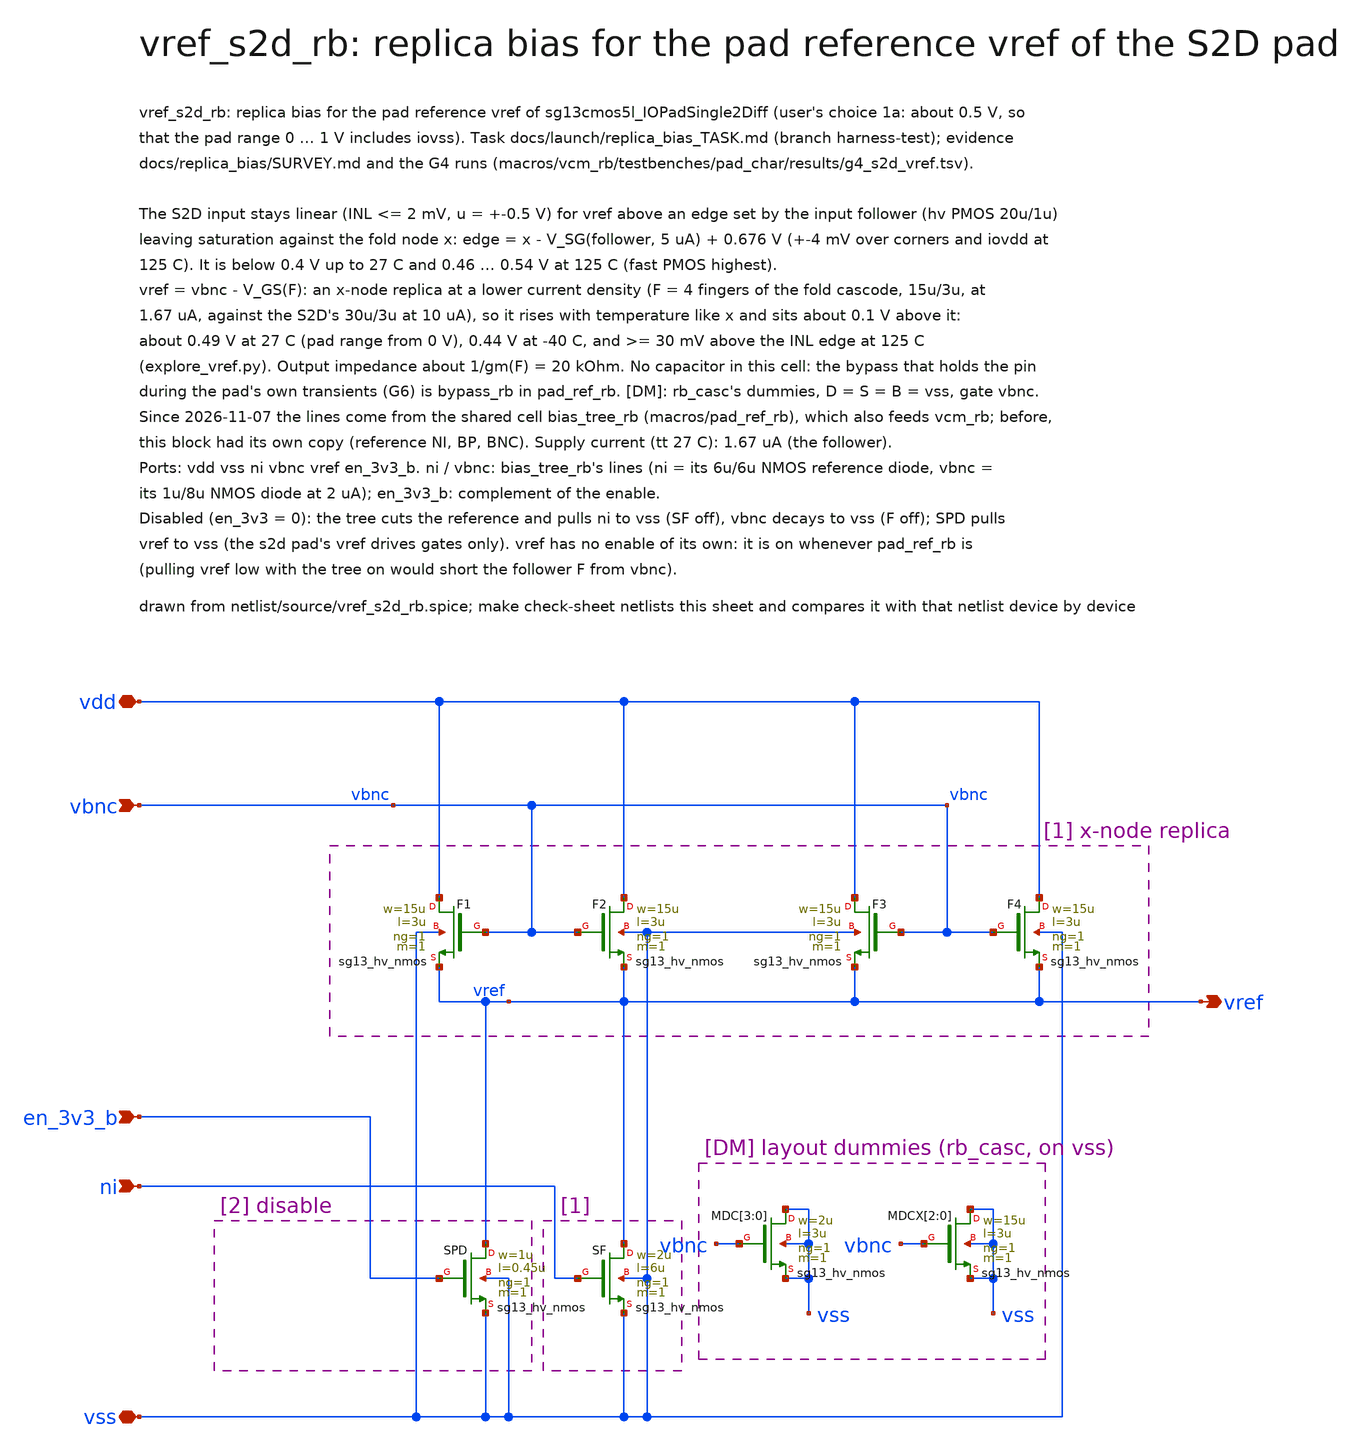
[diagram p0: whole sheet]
** sch_path: macros/vref_s2d_rb/schematic/xschem/vref_s2d_rb.sch
**.subckt vref_s2d_rb vdd vss ni vbnc vref en_3v3_b
*.iopin vdd
*.iopin vss
*.ipin ni
*.ipin vbnc
*.opin vref
*.ipin en_3v3_b
XF1 vdd vbnc vref vss sg13_hv_nmos w=15u l=3u ng=1 m=1 mm_ok=1
XF2 vdd vbnc vref vss sg13_hv_nmos w=15u l=3u ng=1 m=1 mm_ok=1
XF3 vdd vbnc vref vss sg13_hv_nmos w=15u l=3u ng=1 m=1 mm_ok=1
XF4 vdd vbnc vref vss sg13_hv_nmos w=15u l=3u ng=1 m=1 mm_ok=1
XSF vref ni vss vss sg13_hv_nmos w=2u l=6u ng=1 m=1 mm_ok=1
XSPD vref en_3v3_b vss vss sg13_hv_nmos w=1u l=0.45u ng=1 m=1 mm_ok=1
XMDC[3] vss vbnc vss vss sg13_hv_nmos w=2u l=3u ng=1 m=1 mm_ok=1
XMDC[2] vss vbnc vss vss sg13_hv_nmos w=2u l=3u ng=1 m=1 mm_ok=1
XMDC[1] vss vbnc vss vss sg13_hv_nmos w=2u l=3u ng=1 m=1 mm_ok=1
XMDC[0] vss vbnc vss vss sg13_hv_nmos w=2u l=3u ng=1 m=1 mm_ok=1
XMDCX[2] vss vbnc vss vss sg13_hv_nmos w=15u l=3u ng=1 m=1 mm_ok=1
XMDCX[1] vss vbnc vss vss sg13_hv_nmos w=15u l=3u ng=1 m=1 mm_ok=1
XMDCX[0] vss vbnc vss vss sg13_hv_nmos w=15u l=3u ng=1 m=1 mm_ok=1
**.ends
.end
